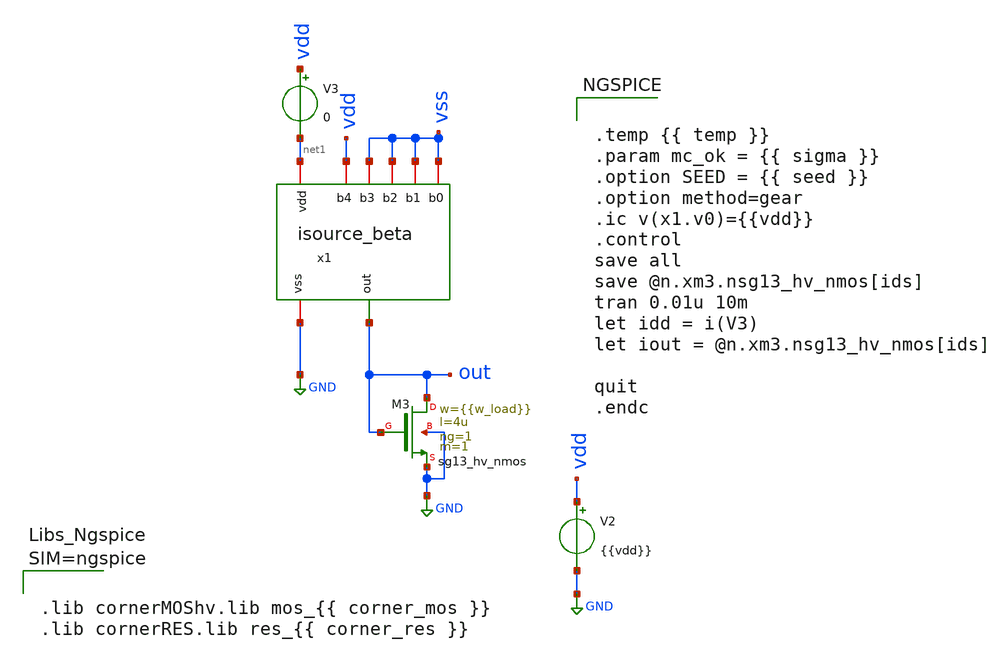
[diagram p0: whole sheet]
** sch_path: testbenches/xschem/tb_isource_beta_tran.sch
**.subckt tb_isource_beta_tran
V2 vdd GND {{vdd}}
V3 vdd net1 0
.save i(v3)
x1 vss net1 vss out vss vss GND vdd isource_beta
XM3 out out GND GND sg13_hv_nmos w={{w_load}} l=4u ng=1 m=1 mm_ok=1
**** begin user architecture code


.temp {{ temp }}
.param mc_ok = {{ sigma }}
.option SEED = {{ seed }}
.option method=gear
.ic v(x1.v0)={{vdd}}
.control
save all
save @n.xm3.nsg13_hv_nmos[ids]
tran 0.01u 10m
let idd = i(V3)
let iout = @n.xm3.nsg13_hv_nmos[ids]

quit
.endc





.lib cornerMOShv.lib mos_{{ corner_mos }}
.lib cornerRES.lib res_{{ corner_res }}



**** end user architecture code
**.ends
.GLOBAL GND
.end
